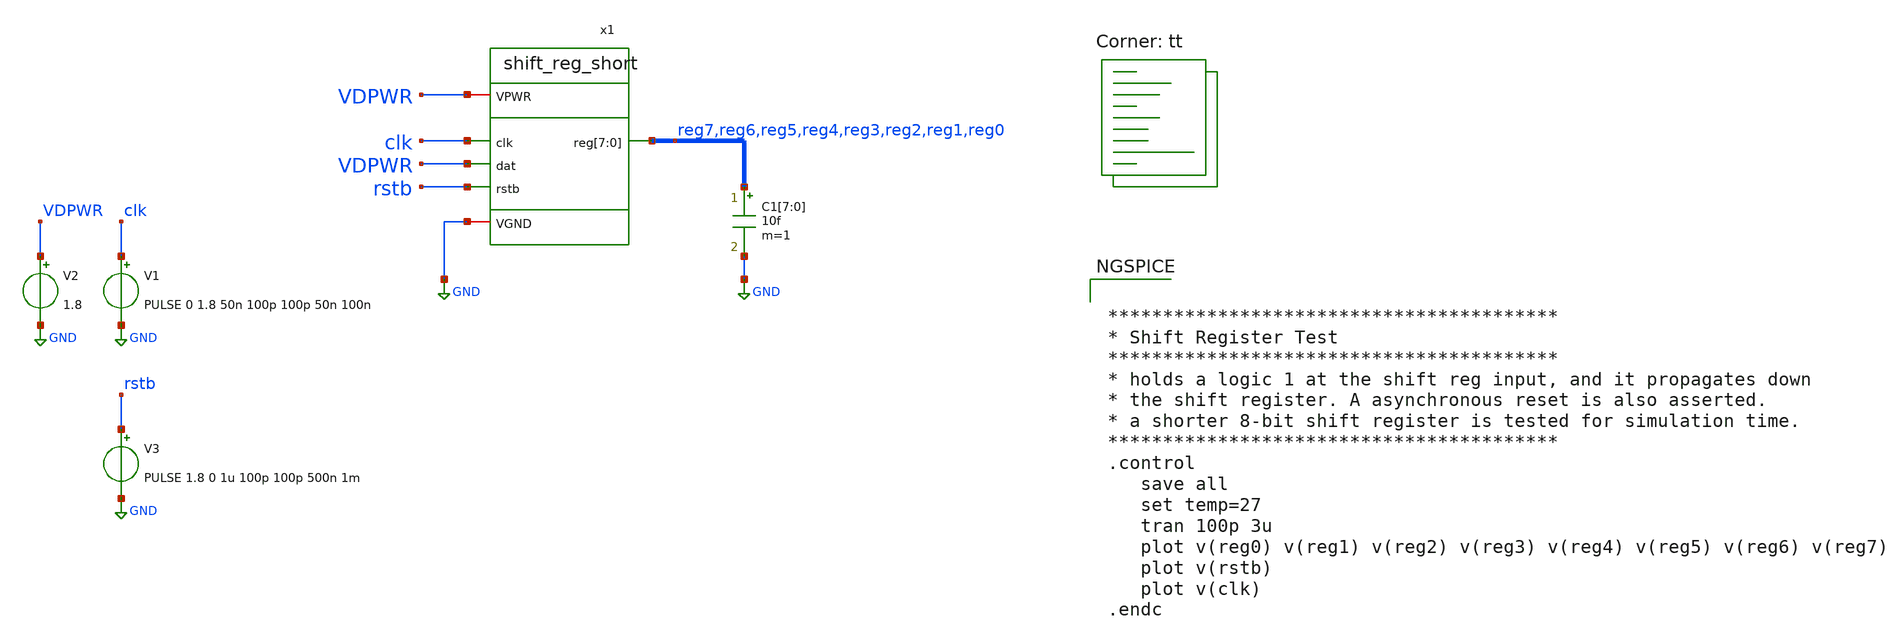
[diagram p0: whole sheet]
** sch_path: xschem/tb_shift_reg.sch
**.subckt tb_shift_reg
V2 VDPWR GND 1.8
C1[7] reg7 GND 10f m=1
C1[6] reg6 GND 10f m=1
C1[5] reg5 GND 10f m=1
C1[4] reg4 GND 10f m=1
C1[3] reg3 GND 10f m=1
C1[2] reg2 GND 10f m=1
C1[1] reg1 GND 10f m=1
C1[0] reg0 GND 10f m=1
V1 clk GND PULSE 0 1.8 50n 100p 100p 50n 100n
V3 rstb GND PULSE 1.8 0 1u 100p 100p 500n 1m
x1 VDPWR clk reg7 reg6 reg5 reg4 reg3 reg2 reg1 reg0 VDPWR rstb GND shift_reg_short
**** begin user architecture code
.lib $::SKYWATER_MODELS/sky130.lib.spice tt


*****************************************
* Shift Register Test
*****************************************
* holds a logic 1 at the shift reg input, and it propagates down
* the shift register. A asynchronous reset is also asserted.
* a shorter 8-bit shift register is tested for simulation time.
*****************************************
.control
   save all
   set temp=27
   tran 100p 3u
   plot v(reg0) v(reg1) v(reg2) v(reg3) v(reg4) v(reg5) v(reg6) v(reg7)
   plot v(rstb)
   plot v(clk)
.endc


**** end user architecture code
**.ends

* expanding   symbol:  shift_reg_short.sym # of pins=6
** sym_path: xschem/shift_reg_short.sym
** sch_path: xschem/shift_reg_short.sch
.subckt shift_reg_short VPWR clk reg[7] reg[6] reg[5] reg[4] reg[3] reg[2] reg[1] reg[0] dat rstb
+ VGND
*.ipin clk
*.ipin dat
*.ipin rstb
*.iopin VPWR
*.iopin VGND
*.opin reg[7],reg[6],reg[5],reg[4],reg[3],reg[2],reg[1],reg[0]
x1[7] clk reg[6] rstb VGND VGND VPWR VPWR reg[7] dff
x1[6] clk reg[5] rstb VGND VGND VPWR VPWR reg[6] dff
x1[5] clk reg[4] rstb VGND VGND VPWR VPWR reg[5] dff
x1[4] clk reg[3] rstb VGND VGND VPWR VPWR reg[4] dff
x1[3] clk reg[2] rstb VGND VGND VPWR VPWR reg[3] dff
x1[2] clk reg[1] rstb VGND VGND VPWR VPWR reg[2] dff
x1[1] clk reg[0] rstb VGND VGND VPWR VPWR reg[1] dff
x1[0] clk dat rstb VGND VGND VPWR VPWR reg[0] dff
.ends


* expanding   symbol:  dff.sym # of pins=8
** sym_path: xschem/dff.sym
** sch_path: xschem/dff.sch
.subckt dff CLK D RESET_B VGND VNB VPB VPWR Q
*.ipin CLK
*.ipin D
*.ipin RESET_B
*.iopin VGND
*.iopin VNB
*.iopin VPB
*.iopin VPWR
*.opin Q
**** begin user architecture code


X0 a_1270_413# a_1283_21# VPWR VPB sky130_fd_pr__pfet_01v8_hvt w=420000u l=150000u
X1 VPWR a_543_47# a_761_289# VPB sky130_fd_pr__pfet_01v8_hvt w=840000u l=150000u
X2 VGND a_543_47# a_761_289# VNB sky130_fd_pr__nfet_01v8 w=640000u l=150000u
X3 VGND D a_448_47# VNB sky130_fd_pr__nfet_01v8 w=420000u l=150000u
X4 a_1108_47# a_193_47# a_1270_413# VPB sky130_fd_pr__pfet_01v8_hvt w=420000u l=150000u
X5 VGND a_1283_21# Q VNB sky130_fd_pr__nfet_01v8 w=650000u l=150000u
X6 a_1217_47# a_1283_21# VGND VNB sky130_fd_pr__nfet_01v8 w=420000u l=150000u
X7 a_448_47# a_27_47# a_543_47# VNB sky130_fd_pr__nfet_01v8 w=360000u l=150000u
X8 a_448_47# a_193_47# a_543_47# VPB sky130_fd_pr__pfet_01v8_hvt w=420000u l=150000u
X9 a_543_47# a_193_47# a_639_47# VNB sky130_fd_pr__nfet_01v8 w=360000u l=150000u
X10 a_1108_47# a_27_47# a_1217_47# VNB sky130_fd_pr__nfet_01v8 w=360000u l=150000u
X11 a_1462_47# a_1108_47# a_1283_21# VNB sky130_fd_pr__nfet_01v8 w=420000u l=150000u
X12 a_543_47# a_27_47# a_651_413# VPB sky130_fd_pr__pfet_01v8_hvt w=420000u l=150000u
X13 a_805_47# RESET_B VGND VNB sky130_fd_pr__nfet_01v8 w=420000u l=150000u
X14 a_761_289# a_193_47# a_1108_47# VNB sky130_fd_pr__nfet_01v8 w=360000u l=150000u
X15 VPWR RESET_B a_651_413# VPB sky130_fd_pr__pfet_01v8_hvt w=420000u l=150000u
X16 VGND a_27_47# a_193_47# VNB sky130_fd_pr__nfet_01v8 w=420000u l=150000u
X17 a_27_47# CLK VGND VNB sky130_fd_pr__nfet_01v8 w=420000u l=150000u
X18 a_27_47# CLK VPWR VPB sky130_fd_pr__pfet_01v8_hvt w=640000u l=150000u
X19 VPWR a_1283_21# Q VPB sky130_fd_pr__pfet_01v8_hvt w=1e+06u l=150000u
X20 VPWR a_27_47# a_193_47# VPB sky130_fd_pr__pfet_01v8_hvt w=640000u l=150000u
X21 a_1283_21# a_1108_47# VPWR VPB sky130_fd_pr__pfet_01v8_hvt w=420000u l=150000u
X22 VGND RESET_B a_1462_47# VNB sky130_fd_pr__nfet_01v8 w=420000u l=150000u
X23 VPWR D a_448_47# VPB sky130_fd_pr__pfet_01v8_hvt w=420000u l=150000u
X24 a_651_413# a_761_289# VPWR VPB sky130_fd_pr__pfet_01v8_hvt w=420000u l=150000u
X25 a_761_289# a_27_47# a_1108_47# VPB sky130_fd_pr__pfet_01v8_hvt w=420000u l=150000u
X26 VPWR RESET_B a_1283_21# VPB sky130_fd_pr__pfet_01v8_hvt w=420000u l=150000u
X27 a_639_47# a_761_289# a_805_47# VNB sky130_fd_pr__nfet_01v8 w=420000u l=150000u


**** end user architecture code
**** begin user architecture code


**** end user architecture code
.ends

.GLOBAL GND
.end
